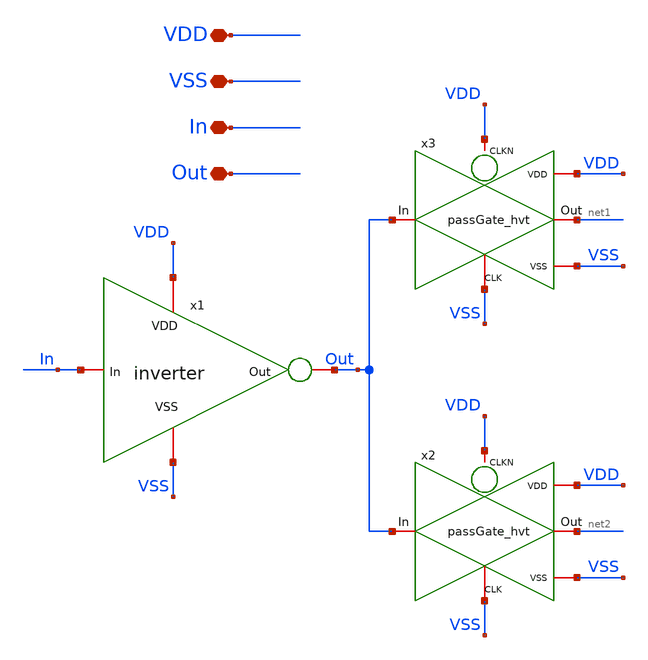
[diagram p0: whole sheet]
** sch_path: HVT/RingStage/RingStage2.sch
**.subckt RingStage2 In Out VDD VSS
*.iopin In
*.iopin Out
*.iopin VDD
*.iopin VSS
x1 VDD Out In VSS inverter
x2 Out VDD VSS VDD VSS net2 passGate_hvt
x3 Out VDD VSS VDD VSS net1 passGate_hvt
**.ends

* expanding   symbol:  /foss/designs/RO_Aging_UNICASS/HVT/inverter/inverter.sym # of pins=4
** sym_path: MUX/inverter.sym
** sch_path: MUX/inverter.sch
.subckt inverter VDD Out In VSS
*.iopin VDD
*.iopin Out
*.iopin VSS
*.iopin In
XM3 Out In VSS VSS sky130_fd_pr__nfet_01v8 L=0.15 W=2.1 nf=1 ad='int((nf+1)/2) * W/nf * 0.29' as='int((nf+2)/2) * W/nf * 0.29'
+ pd='2*int((nf+1)/2) * (W/nf + 0.29)' ps='2*int((nf+2)/2) * (W/nf + 0.29)' nrd='0.29 / W' nrs='0.29 / W'
+ sa=0 sb=0 sd=0 mult=2 m=2
XM1 Out In VDD VDD sky130_fd_pr__pfet_01v8 L=0.15 W=4.75 nf=1 ad='int((nf+1)/2) * W/nf * 0.29' as='int((nf+2)/2) * W/nf * 0.29'
+ pd='2*int((nf+1)/2) * (W/nf + 0.29)' ps='2*int((nf+2)/2) * (W/nf + 0.29)' nrd='0.29 / W' nrs='0.29 / W'
+ sa=0 sb=0 sd=0 mult=4 m=4
.ends


* expanding   symbol:  /foss/designs/RO_Aging_UNICASS/HVT/passGate_hvt/passGate_hvt.sym # of pins=6
** sym_path: HVT/passGate_hvt/passGate_hvt.sym
** sch_path: HVT/passGate_hvt/passGate_hvt.sch
.subckt passGate_hvt In CLKN VSS VDD CLK Out
*.iopin In
*.iopin CLKN
*.iopin Out
*.iopin VSS
*.iopin VDD
*.iopin CLK
XM2 Out CLKN In VDD sky130_fd_pr__pfet_01v8_hvt L=0.15 W=0.45 nf=1 ad='int((nf+1)/2) * W/nf * 0.29' as='int((nf+2)/2) * W/nf * 0.29'
+ pd='2*int((nf+1)/2) * (W/nf + 0.29)' ps='2*int((nf+2)/2) * (W/nf + 0.29)' nrd='0.29 / W' nrs='0.29 / W'
+ sa=0 sb=0 sd=0 mult=1 m=1
XM1 Out CLK In VSS sky130_fd_pr__nfet_01v8 L=0.15 W=0.45 nf=1 ad='int((nf+1)/2) * W/nf * 0.29' as='int((nf+2)/2) * W/nf * 0.29'
+ pd='2*int((nf+1)/2) * (W/nf + 0.29)' ps='2*int((nf+2)/2) * (W/nf + 0.29)' nrd='0.29 / W' nrs='0.29 / W'
+ sa=0 sb=0 sd=0 mult=1 m=1
.ends

.end
